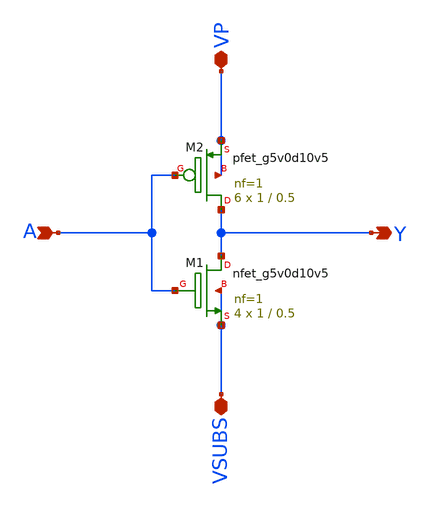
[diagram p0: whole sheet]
** sch_path: xschem/inv_x6.sch
**.subckt inv_x6 VP VSUBS A Y
*.iopin VP
*.iopin VSUBS
*.ipin A
*.opin Y
XM1 Y A VSUBS VSUBS sky130_fd_pr__nfet_g5v0d10v5 L=0.5 W=1 nf=1 ad='int((nf+1)/2) * W/nf * 0.29' as='int((nf+2)/2) * W/nf * 0.29'
+ pd='2*int((nf+1)/2) * (W/nf + 0.29)' ps='2*int((nf+2)/2) * (W/nf + 0.29)' nrd='0.29 / W' nrs='0.29 / W'
+ sa=0 sb=0 sd=0 mult=4 m=4
XM2 Y A VP VP sky130_fd_pr__pfet_g5v0d10v5 L=0.5 W=1 nf=1 ad='int((nf+1)/2) * W/nf * 0.29' as='int((nf+2)/2) * W/nf * 0.29'
+ pd='2*int((nf+1)/2) * (W/nf + 0.29)' ps='2*int((nf+2)/2) * (W/nf + 0.29)' nrd='0.29 / W' nrs='0.29 / W'
+ sa=0 sb=0 sd=0 mult=6 m=6
**.ends
.end
